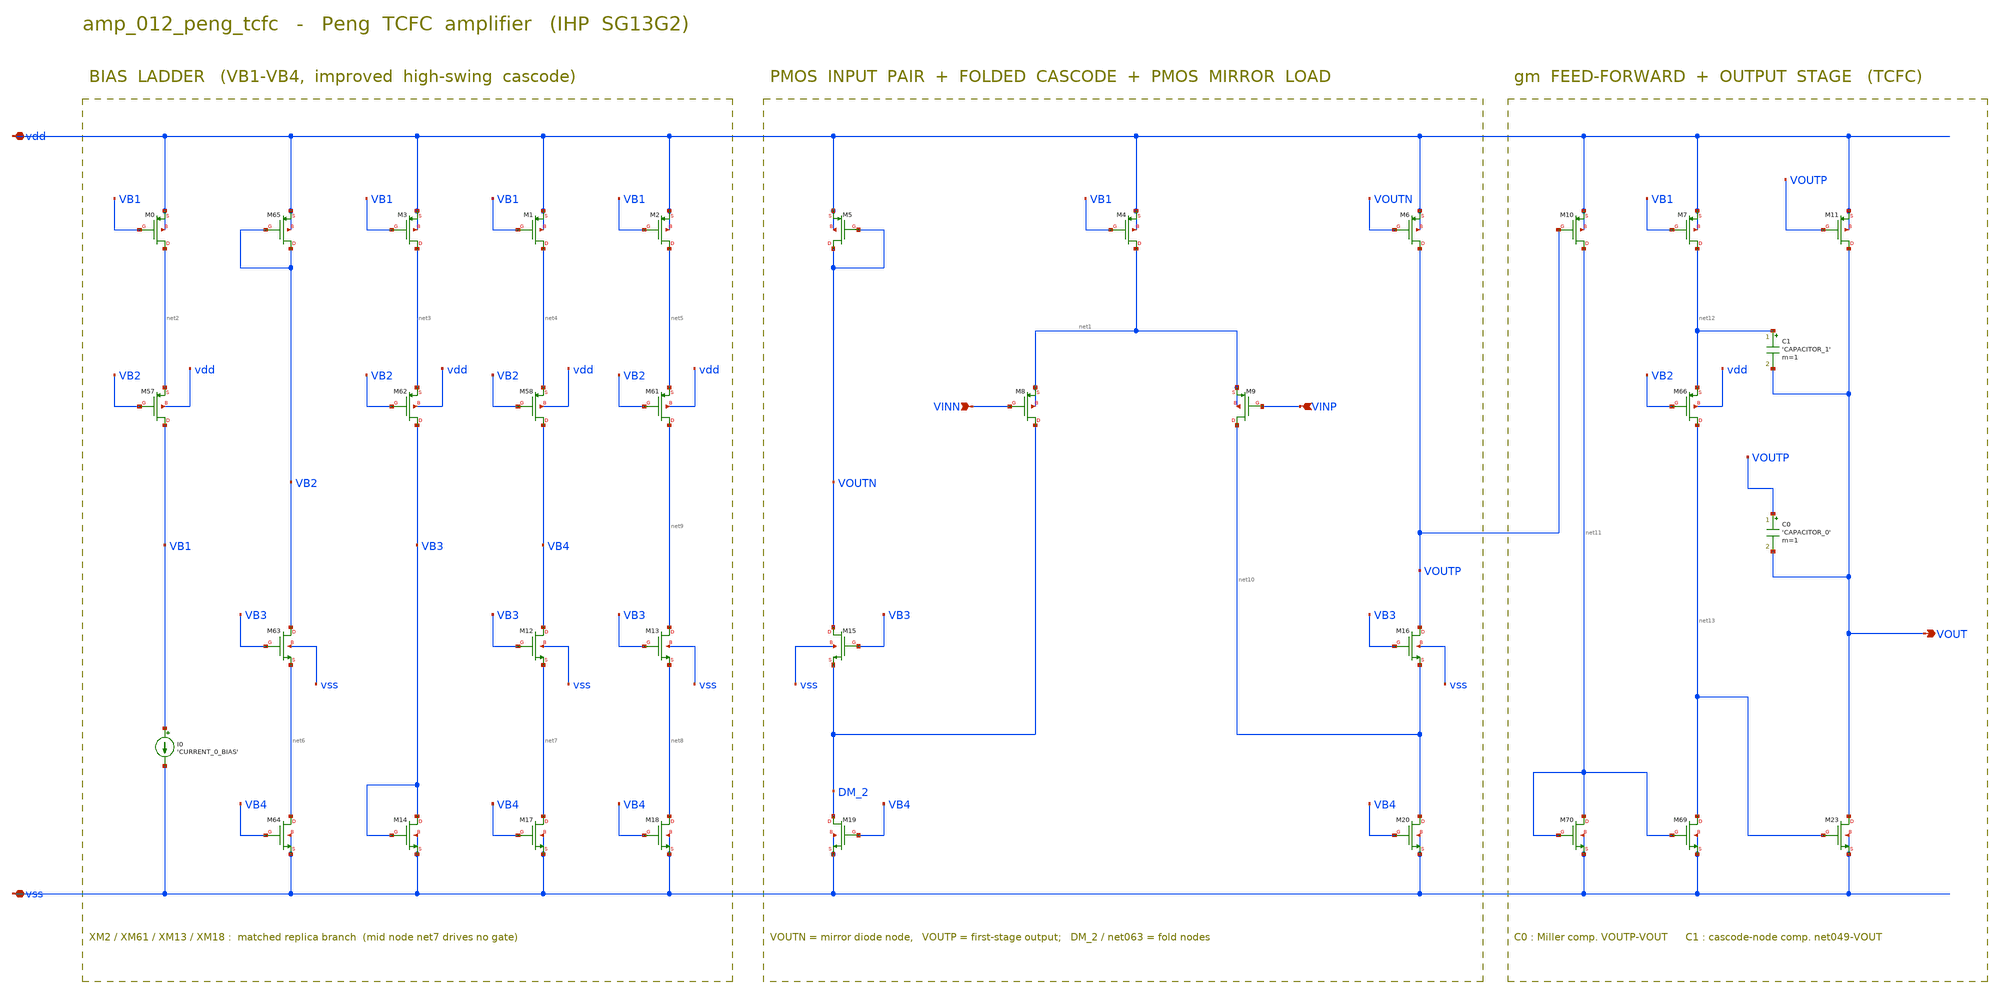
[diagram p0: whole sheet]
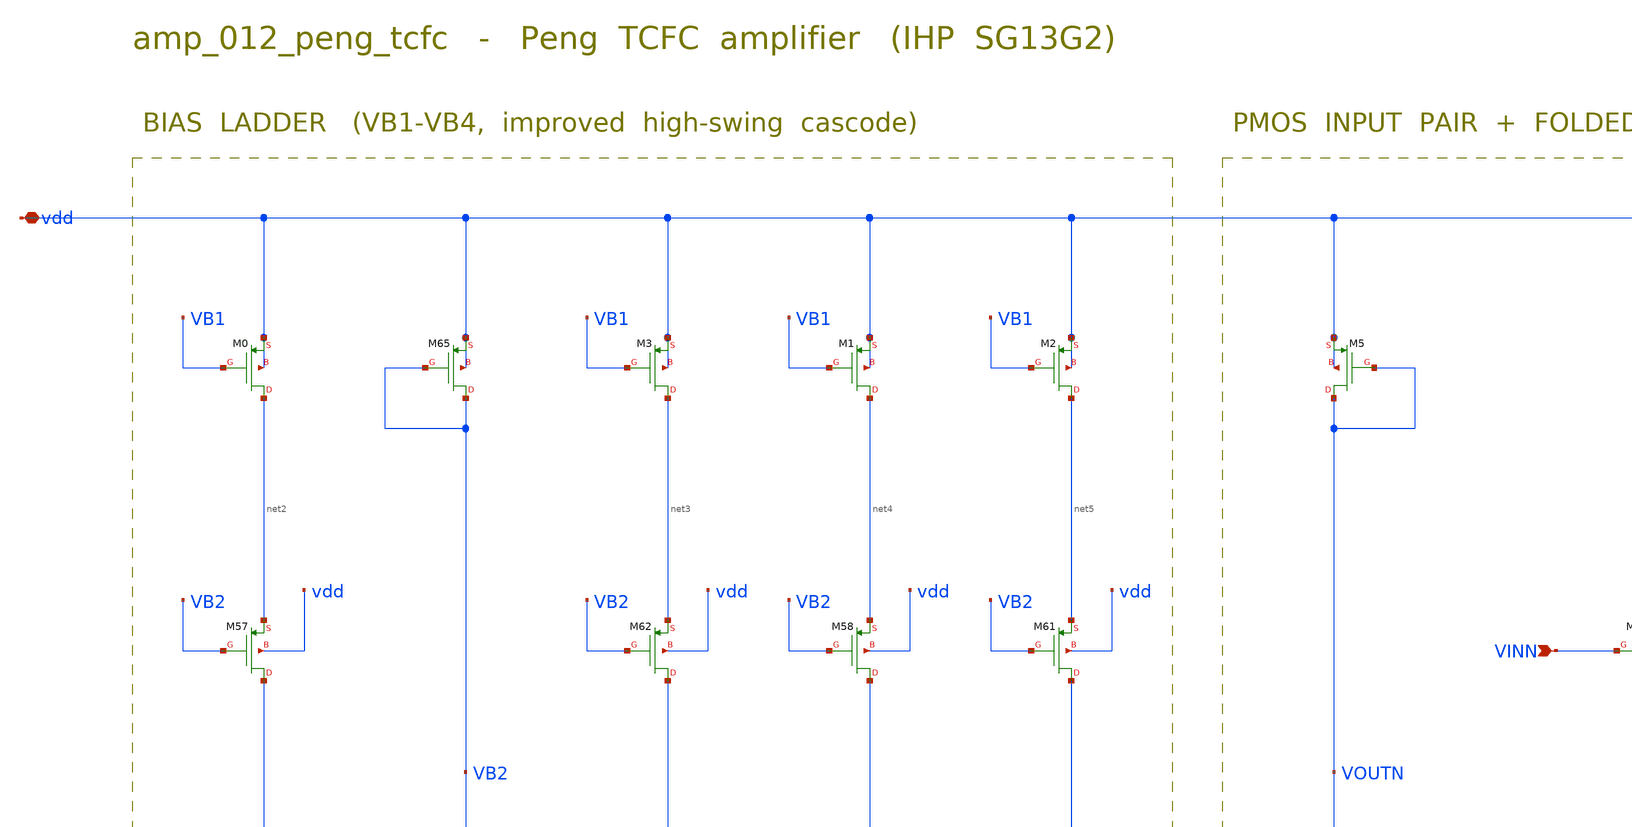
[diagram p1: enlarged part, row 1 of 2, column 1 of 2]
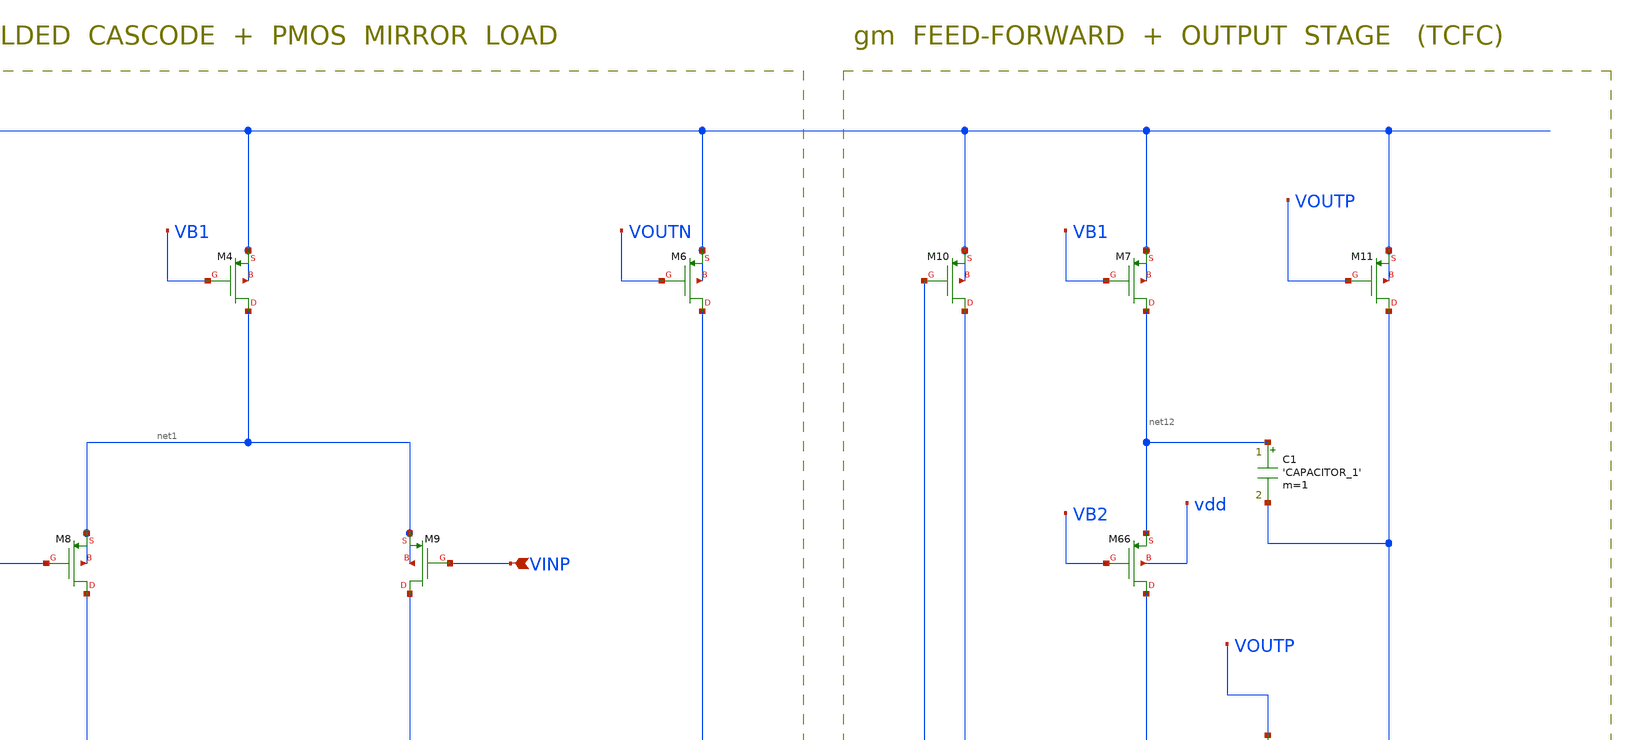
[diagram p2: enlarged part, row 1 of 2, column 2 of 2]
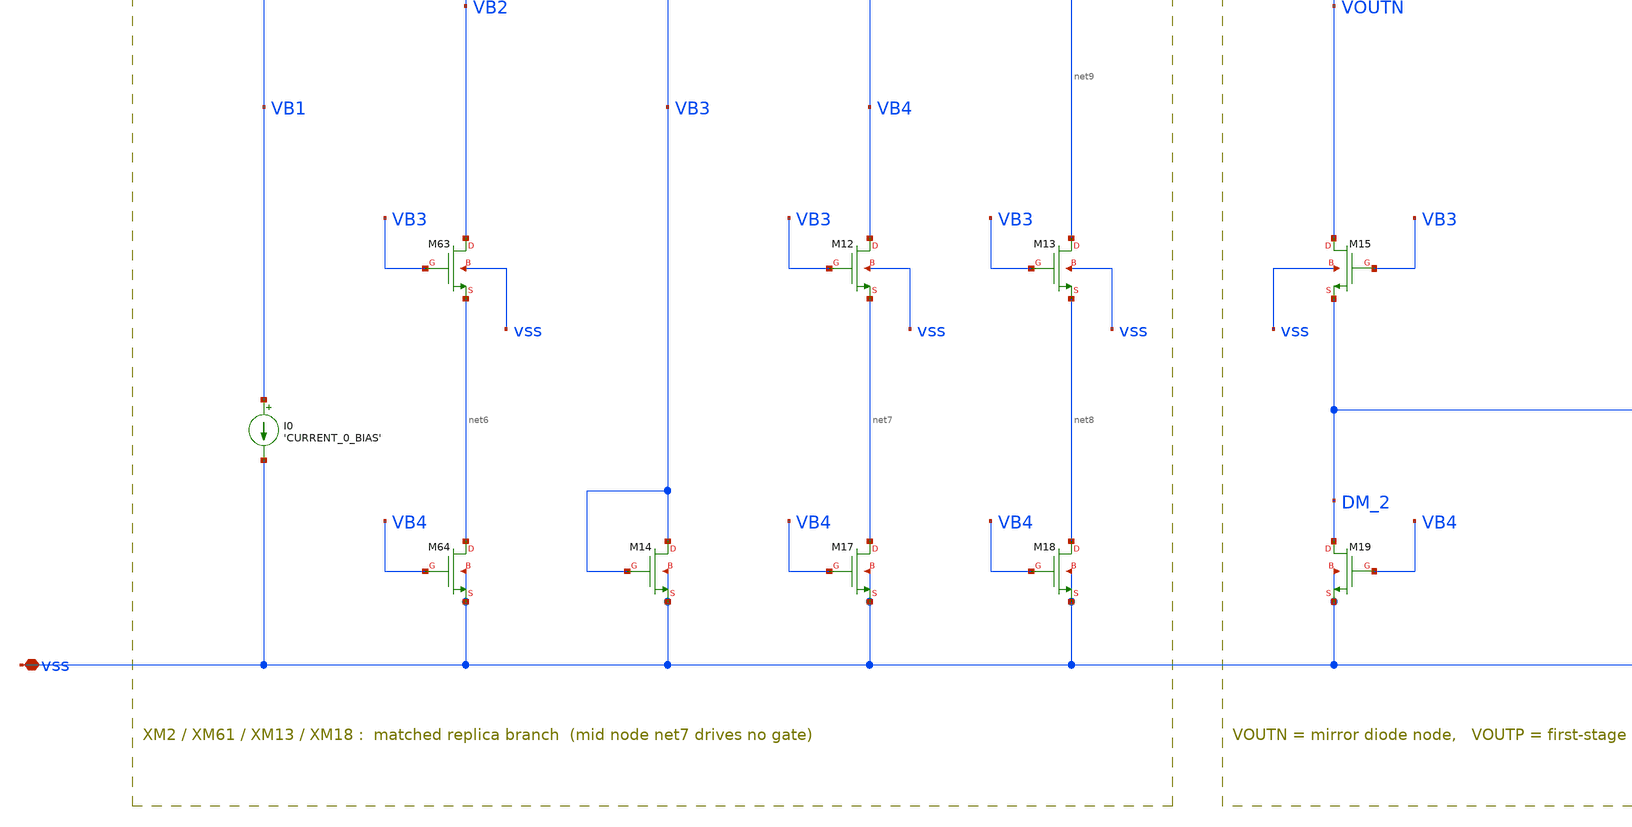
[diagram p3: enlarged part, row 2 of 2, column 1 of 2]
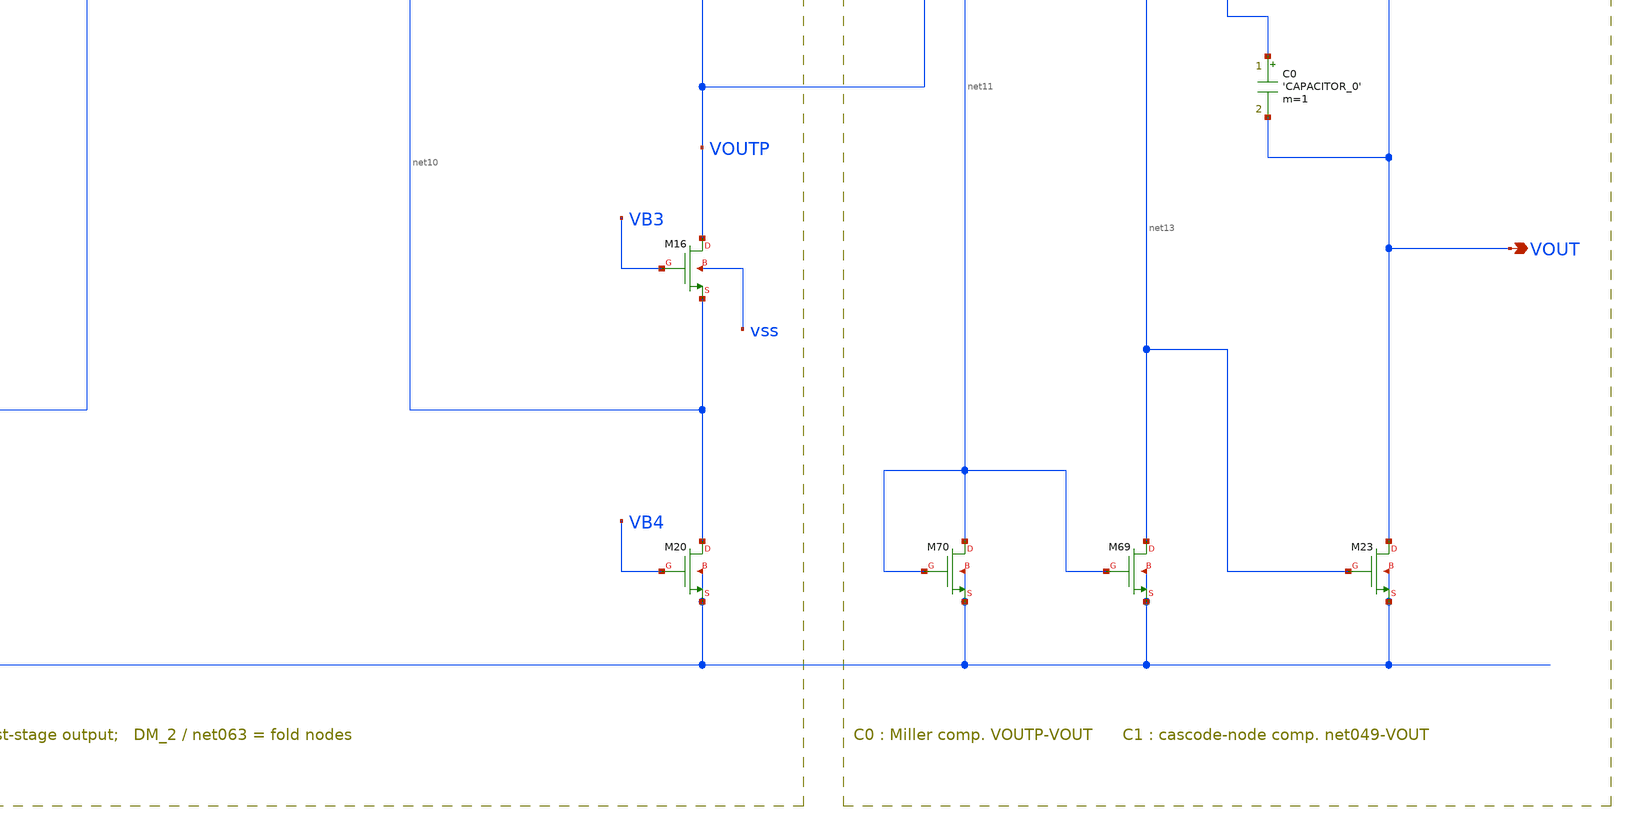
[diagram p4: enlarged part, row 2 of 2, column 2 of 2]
** sch_path: analog-db/drawings/publication/amp_012_peng_tcfc.sch
**.subckt amp_012_peng_tcfc vss vdd VINN VINP VOUT
*.iopin vss
*.iopin vdd
*.ipin VINN
*.ipin VINP
*.opin VOUT
XM0 net2 VB1 vdd vdd sg13_lv_pmos w=x_dut_xm0_w l=x_dut_xm0_l ng=1 m=x_dut_xm0_m
XM57 VB1 VB2 net2 vdd sg13_lv_pmos w=x_dut_xm57_w l=x_dut_xm57_l ng=1 m=x_dut_xm57_m
XM65 VB2 VB2 vdd vdd sg13_lv_pmos w=x_dut_xm65_w l=x_dut_xm65_l ng=1 m=x_dut_xm65_m
XM63 VB2 VB3 net6 vss sg13_lv_nmos w=x_dut_xm63_w l=x_dut_xm63_l ng=1 m=x_dut_xm63_m
XM64 net6 VB4 vss vss sg13_lv_nmos w=x_dut_xm64_w l=x_dut_xm64_l ng=1 m=x_dut_xm64_m
XM3 net3 VB1 vdd vdd sg13_lv_pmos w=x_dut_xm3_w l=x_dut_xm3_l ng=1 m=x_dut_xm3_m
XM62 VB3 VB2 net3 vdd sg13_lv_pmos w=x_dut_xm62_w l=x_dut_xm62_l ng=1 m=x_dut_xm62_m
XM14 VB3 VB3 vss vss sg13_lv_nmos w=x_dut_xm14_w l=x_dut_xm14_l ng=1 m=x_dut_xm14_m
XM1 net4 VB1 vdd vdd sg13_lv_pmos w=x_dut_xm1_w l=x_dut_xm1_l ng=1 m=x_dut_xm1_m
XM58 VB4 VB2 net4 vdd sg13_lv_pmos w=x_dut_xm58_w l=x_dut_xm58_l ng=1 m=x_dut_xm58_m
XM12 VB4 VB3 net7 vss sg13_lv_nmos w=x_dut_xm12_w l=x_dut_xm12_l ng=1 m=x_dut_xm12_m
XM17 net7 VB4 vss vss sg13_lv_nmos w=x_dut_xm17_w l=x_dut_xm17_l ng=1 m=x_dut_xm17_m
XM2 net5 VB1 vdd vdd sg13_lv_pmos w=x_dut_xm2_w l=x_dut_xm2_l ng=1 m=x_dut_xm2_m
XM61 net9 VB2 net5 vdd sg13_lv_pmos w=x_dut_xm61_w l=x_dut_xm61_l ng=1 m=x_dut_xm61_m
XM13 net9 VB3 net8 vss sg13_lv_nmos w=x_dut_xm13_w l=x_dut_xm13_l ng=1 m=x_dut_xm13_m
XM18 net8 VB4 vss vss sg13_lv_nmos w=x_dut_xm18_w l=x_dut_xm18_l ng=1 m=x_dut_xm18_m
XM5 VOUTN VOUTN vdd vdd sg13_lv_pmos w=x_dut_xm5_w l=x_dut_xm5_l ng=1 m=x_dut_xm5_m
XM15 VOUTN VB3 DM_2 vss sg13_lv_nmos w=x_dut_xm15_w l=x_dut_xm15_l ng=1 m=x_dut_xm15_m
XM19 DM_2 VB4 vss vss sg13_lv_nmos w=x_dut_xm19_w l=x_dut_xm19_l ng=1 m=x_dut_xm19_m
XM8 DM_2 VINN net1 net1 sg13_lv_pmos w=x_dut_xm8_w l=x_dut_xm8_l ng=1 m=x_dut_xm8_m
XM4 net1 VB1 vdd vdd sg13_lv_pmos w=x_dut_xm4_w l=x_dut_xm4_l ng=1 m=x_dut_xm4_m
XM9 net10 VINP net1 net1 sg13_lv_pmos w=x_dut_xm9_w l=x_dut_xm9_l ng=1 m=x_dut_xm9_m
XM6 VOUTP VOUTN vdd vdd sg13_lv_pmos w=x_dut_xm6_w l=x_dut_xm6_l ng=1 m=x_dut_xm6_m
XM16 VOUTP VB3 net10 vss sg13_lv_nmos w=x_dut_xm16_w l=x_dut_xm16_l ng=1 m=x_dut_xm16_m
XM20 net10 VB4 vss vss sg13_lv_nmos w=x_dut_xm20_w l=x_dut_xm20_l ng=1 m=x_dut_xm20_m
XM10 net11 VOUTP vdd vdd sg13_lv_pmos w=x_dut_xm10_w l=x_dut_xm10_l ng=1 m=x_dut_xm10_m
XM70 net11 net11 vss vss sg13_lv_nmos w=x_dut_xm70_w l=x_dut_xm70_l ng=1 m=x_dut_xm70_m
XM7 net12 VB1 vdd vdd sg13_lv_pmos w=x_dut_xm7_w l=x_dut_xm7_l ng=1 m=x_dut_xm7_m
XM66 net13 VB2 net12 vdd sg13_lv_pmos w=x_dut_xm66_w l=x_dut_xm66_l ng=1 m=x_dut_xm66_m
XM69 net13 net11 vss vss sg13_lv_nmos w=x_dut_xm69_w l=x_dut_xm69_l ng=1 m=x_dut_xm69_m
XM11 VOUT VOUTP vdd vdd sg13_lv_pmos w=x_dut_xm11_w l=x_dut_xm11_l ng=1 m=x_dut_xm11_m
XM23 VOUT net13 vss vss sg13_lv_nmos w=x_dut_xm23_w l=x_dut_xm23_l ng=1 m=x_dut_xm23_m
I0 VB1 vss 'CURRENT_0_BIAS'
C0 VOUTP VOUT 'CAPACITOR_0' m=1
C1 net12 VOUT 'CAPACITOR_1' m=1
**.ends
.end
